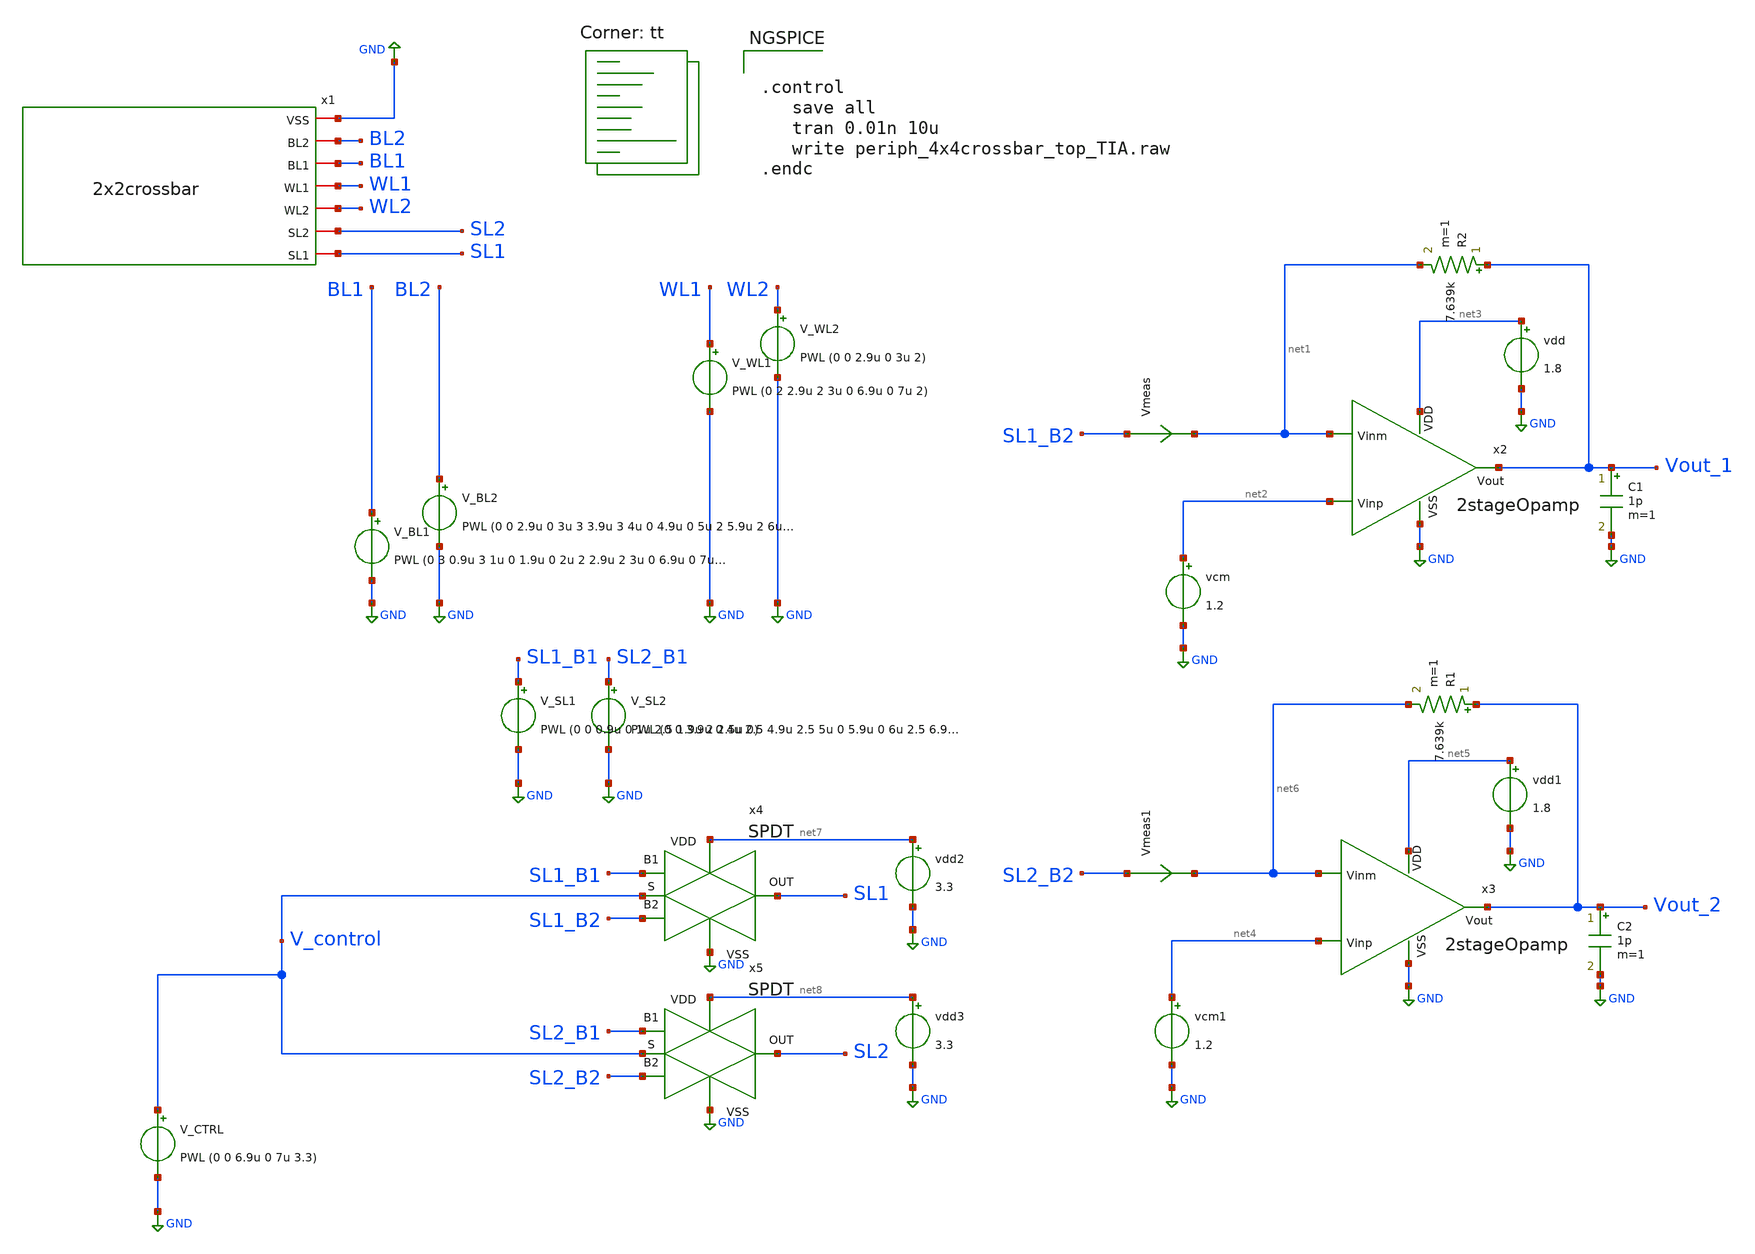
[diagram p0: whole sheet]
** sch_path: xschem/test/xschem/periph_4x4crossbar_top_TIA.sch
* StefanSchippers/xschem_sky130/sky130_fd_pr/reram.sym:
* Copyright 2021 Stefan Frederik Schippers
* Licensed under the Apache License, Version 2.0 (the "License");
**.subckt periph_4x4crossbar_top_TIA
V_BL1 BL1 GND PWL (0 3 0.9u 3 1u 0 1.9u 0 2u 2 2.9u 2 3u 0 6.9u 0 7u 0.2)
V_BL2 BL2 GND PWL (0 0 2.9u 0 3u 3 3.9u 3 4u 0 4.9u 0 5u 2 5.9u 2 6u 0 6.9u 0 7u 0.2)
x1 GND BL2 BL1 WL1 WL2 SL2 SL1 2x2crossbar
V_SL1 SL1_B1 GND PWL (0 0 0.9u 0 1u 2.5 1.9u 2 2.5u 0)
V_SL2 SL2_B1 GND PWL (0 0 3.9u 0 4u 2.5 4.9u 2.5 5u 0 5.9u 0 6u 2.5 6.9u 2.5 7u 0)
V_WL1 WL1 GND PWL (0 2 2.9u 2 3u 0 6.9u 0 7u 2)
V_WL2 WL2 GND PWL (0 0 2.9u 0 3u 2)
x2 net3 net1 net2 Vout_1 GND 2stageOpamp
vcm net2 GND 1.2
vdd net3 GND 1.8
C1 Vout_1 GND 1p m=1
R2 Vout_1 net1 7.639k m=1
x3 net5 net6 net4 Vout_2 GND 2stageOpamp
vcm1 net4 GND 1.2
vdd1 net5 GND 1.8
C2 Vout_2 GND 1p m=1
R1 Vout_2 net6 7.639k m=1
x4 net7 GND SL1_B2 V_control SL1_B1 SL1 SPDT
x5 net8 GND SL2_B2 V_control SL2_B1 SL2 SPDT
V_CTRL V_control GND PWL (0 0 6.9u 0 7u 3.3)
vdd2 net7 GND 3.3
vdd3 net8 GND 3.3
Vmeas SL1_B2 net1 0
.save i(vmeas)
Vmeas1 SL2_B2 net6 0
.save i(vmeas1)
**** begin user architecture code
.lib $::SKYWATER_MODELS/sky130.lib.spice tt


.control
   save all
   tran 0.01n 10u
   write periph_4x4crossbar_top_TIA.raw
.endc


**** end user architecture code
**.ends

* expanding   symbol:  2x2crossbar.sym # of pins=7
** sym_path: 2x2crossbar.sym
** sch_path: 2x2crossbar.sch
.subckt 2x2crossbar VSS BL2 BL1 WL1 WL2 SL2 SL1
*.iopin BL2
*.iopin BL1
*.iopin WL1
*.iopin WL2
*.iopin SL1
*.iopin SL2
*.iopin VSS
x1 BL1 WL1 SL1 VSS 1T1R
x2 BL2 WL1 SL2 VSS 1T1R
x3 BL1 WL2 SL1 VSS 1T1R
x4 BL2 WL2 SL2 VSS 1T1R
.ends


* expanding   symbol:  amplifiers/dec24/2stageOpamp.sym # of pins=5
** sym_path: amplifiers/dec24/2stageOpamp.sym
** sch_path: amplifiers/dec24/2stageOpamp.sch
.subckt 2stageOpamp VDD Vinm Vinp Vout VSS
*.ipin Vinm
*.ipin Vinp
*.opin Vout
*.ipin VSS
*.ipin VDD
XM8 Vout net1 VSS VSS sky130_fd_pr__nfet_01v8 L=1 W=6 nf=1 ad='int((nf+1)/2) * W/nf * 0.29' as='int((nf+2)/2) * W/nf * 0.29'
+ pd='2*int((nf+1)/2) * (W/nf + 0.29)' ps='2*int((nf+2)/2) * (W/nf + 0.29)' nrd='0.29 / W' nrs='0.29 / W'
+ sa=0 sb=0 sd=0 mult=8 m=8
XM2 Vout Vb1 VDD VDD sky130_fd_pr__pfet_01v8_lvt L=1 W=9 nf=1 ad='int((nf+1)/2) * W/nf * 0.29' as='int((nf+2)/2) * W/nf * 0.29'
+ pd='2*int((nf+1)/2) * (W/nf + 0.29)' ps='2*int((nf+2)/2) * (W/nf + 0.29)' nrd='0.29 / W' nrs='0.29 / W'
+ sa=0 sb=0 sd=0 mult=3 m=3
XM5 net5 Vb3 net6 VSS sky130_fd_pr__nfet_01v8 L=1 W=4 nf=1 ad='int((nf+1)/2) * W/nf * 0.29' as='int((nf+2)/2) * W/nf * 0.29'
+ pd='2*int((nf+1)/2) * (W/nf + 0.29)' ps='2*int((nf+2)/2) * (W/nf + 0.29)' nrd='0.29 / W' nrs='0.29 / W'
+ sa=0 sb=0 sd=0 mult=3 m=3
XM17 net1 Vb3 net7 VSS sky130_fd_pr__nfet_01v8 L=1 W=4 nf=1 ad='int((nf+1)/2) * W/nf * 0.29' as='int((nf+2)/2) * W/nf * 0.29'
+ pd='2*int((nf+1)/2) * (W/nf + 0.29)' ps='2*int((nf+2)/2) * (W/nf + 0.29)' nrd='0.29 / W' nrs='0.29 / W'
+ sa=0 sb=0 sd=0 mult=3 m=3
XM3 net6 net5 VSS VSS sky130_fd_pr__nfet_01v8 L=1 W=8 nf=1 ad='int((nf+1)/2) * W/nf * 0.29' as='int((nf+2)/2) * W/nf * 0.29'
+ pd='2*int((nf+1)/2) * (W/nf + 0.29)' ps='2*int((nf+2)/2) * (W/nf + 0.29)' nrd='0.29 / W' nrs='0.29 / W'
+ sa=0 sb=0 sd=0 mult=1 m=1
XM19 net7 net5 VSS VSS sky130_fd_pr__nfet_01v8 L=1 W=8 nf=1 ad='int((nf+1)/2) * W/nf * 0.29' as='int((nf+2)/2) * W/nf * 0.29'
+ pd='2*int((nf+1)/2) * (W/nf + 0.29)' ps='2*int((nf+2)/2) * (W/nf + 0.29)' nrd='0.29 / W' nrs='0.29 / W'
+ sa=0 sb=0 sd=0 mult=1 m=1
V1 Vb1 GND 1.1
V2 Vb2 GND 0.7
V3 Vb3 GND 0.9
XM11 net8 Vb1 VDD VDD sky130_fd_pr__pfet_01v8_lvt L=1 W=9 nf=1 ad='int((nf+1)/2) * W/nf * 0.29' as='int((nf+2)/2) * W/nf * 0.29'
+ pd='2*int((nf+1)/2) * (W/nf + 0.29)' ps='2*int((nf+2)/2) * (W/nf + 0.29)' nrd='0.29 / W' nrs='0.29 / W'
+ sa=0 sb=0 sd=0 mult=2 m=2
XM1 net6 Vinm net8 VDD sky130_fd_pr__pfet_01v8_lvt L=1 W=8 nf=1 ad='int((nf+1)/2) * W/nf * 0.29' as='int((nf+2)/2) * W/nf * 0.29'
+ pd='2*int((nf+1)/2) * (W/nf + 0.29)' ps='2*int((nf+2)/2) * (W/nf + 0.29)' nrd='0.29 / W' nrs='0.29 / W'
+ sa=0 sb=0 sd=0 mult=3 m=3
XM15 net7 Vinp net8 VDD sky130_fd_pr__pfet_01v8_lvt L=1 W=8 nf=1 ad='int((nf+1)/2) * W/nf * 0.29' as='int((nf+2)/2) * W/nf * 0.29'
+ pd='2*int((nf+1)/2) * (W/nf + 0.29)' ps='2*int((nf+2)/2) * (W/nf + 0.29)' nrd='0.29 / W' nrs='0.29 / W'
+ sa=0 sb=0 sd=0 mult=3 m=3
XM7 net3 Vb1 VDD VDD sky130_fd_pr__pfet_01v8_lvt L=1 W=9 nf=1 ad='int((nf+1)/2) * W/nf * 0.29' as='int((nf+2)/2) * W/nf * 0.29'
+ pd='2*int((nf+1)/2) * (W/nf + 0.29)' ps='2*int((nf+2)/2) * (W/nf + 0.29)' nrd='0.29 / W' nrs='0.29 / W'
+ sa=0 sb=0 sd=0 mult=1 m=1
XM21 net4 Vb1 VDD VDD sky130_fd_pr__pfet_01v8_lvt L=1 W=9 nf=1 ad='int((nf+1)/2) * W/nf * 0.29' as='int((nf+2)/2) * W/nf * 0.29'
+ pd='2*int((nf+1)/2) * (W/nf + 0.29)' ps='2*int((nf+2)/2) * (W/nf + 0.29)' nrd='0.29 / W' nrs='0.29 / W'
+ sa=0 sb=0 sd=0 mult=1 m=1
XM9 net5 Vb2 net3 VDD sky130_fd_pr__pfet_01v8_lvt L=1 W=9 nf=1 ad='int((nf+1)/2) * W/nf * 0.29' as='int((nf+2)/2) * W/nf * 0.29'
+ pd='2*int((nf+1)/2) * (W/nf + 0.29)' ps='2*int((nf+2)/2) * (W/nf + 0.29)' nrd='0.29 / W' nrs='0.29 / W'
+ sa=0 sb=0 sd=0 mult=1 m=1
XM23 net1 Vb2 net4 VDD sky130_fd_pr__pfet_01v8_lvt L=1 W=9 nf=1 ad='int((nf+1)/2) * W/nf * 0.29' as='int((nf+2)/2) * W/nf * 0.29'
+ pd='2*int((nf+1)/2) * (W/nf + 0.29)' ps='2*int((nf+2)/2) * (W/nf + 0.29)' nrd='0.29 / W' nrs='0.29 / W'
+ sa=0 sb=0 sd=0 mult=1 m=1
XC4 net2 Vout sky130_fd_pr__cap_mim_m3_2 W=7 L=7 MF=4 m=4
R4 net1 net2 7k m=1
.ends


* expanding   symbol:  SPDT.sym # of pins=6
** sym_path: xschem/test/xschem/SPDT.sym
** sch_path: xschem/test/xschem/SPDT.sch
.subckt SPDT VDD VSS B2 S B1 OUT
*.ipin S
*.ipin VDD
*.ipin VSS
*.iopin OUT
*.iopin B1
*.iopin B2
XM1 OUT net1 B2 VSS sky130_fd_pr__nfet_g5v0d10v5 L=0.5 W=15 nf=1 ad='int((nf+1)/2) * W/nf * 0.29' as='int((nf+2)/2) * W/nf * 0.29'
+ pd='2*int((nf+1)/2) * (W/nf + 0.29)' ps='2*int((nf+2)/2) * (W/nf + 0.29)' nrd='0.29 / W' nrs='0.29 / W'
+ sa=0 sb=0 sd=0 mult=1 m=1
XM2 B2 net2 OUT VDD sky130_fd_pr__pfet_g5v0d10v5 L=0.5 W=15 nf=1 ad='int((nf+1)/2) * W/nf * 0.29' as='int((nf+2)/2) * W/nf * 0.29'
+ pd='2*int((nf+1)/2) * (W/nf + 0.29)' ps='2*int((nf+2)/2) * (W/nf + 0.29)' nrd='0.29 / W' nrs='0.29 / W'
+ sa=0 sb=0 sd=0 mult=1 m=1
XM3 OUT net2 B1 VSS sky130_fd_pr__nfet_g5v0d10v5 L=0.5 W=15 nf=1 ad='int((nf+1)/2) * W/nf * 0.29' as='int((nf+2)/2) * W/nf * 0.29'
+ pd='2*int((nf+1)/2) * (W/nf + 0.29)' ps='2*int((nf+2)/2) * (W/nf + 0.29)' nrd='0.29 / W' nrs='0.29 / W'
+ sa=0 sb=0 sd=0 mult=1 m=1
XM4 B1 net1 OUT VDD sky130_fd_pr__pfet_g5v0d10v5 L=0.5 W=15 nf=1 ad='int((nf+1)/2) * W/nf * 0.29' as='int((nf+2)/2) * W/nf * 0.29'
+ pd='2*int((nf+1)/2) * (W/nf + 0.29)' ps='2*int((nf+2)/2) * (W/nf + 0.29)' nrd='0.29 / W' nrs='0.29 / W'
+ sa=0 sb=0 sd=0 mult=1 m=1
XM5 net2 S VSS VSS sky130_fd_pr__nfet_g5v0d10v5 L=0.5 W=1 nf=1 ad='int((nf+1)/2) * W/nf * 0.29' as='int((nf+2)/2) * W/nf * 0.29'
+ pd='2*int((nf+1)/2) * (W/nf + 0.29)' ps='2*int((nf+2)/2) * (W/nf + 0.29)' nrd='0.29 / W' nrs='0.29 / W'
+ sa=0 sb=0 sd=0 mult=1 m=1
XM6 net2 S VDD VDD sky130_fd_pr__pfet_g5v0d10v5 L=0.5 W=1 nf=1 ad='int((nf+1)/2) * W/nf * 0.29' as='int((nf+2)/2) * W/nf * 0.29'
+ pd='2*int((nf+1)/2) * (W/nf + 0.29)' ps='2*int((nf+2)/2) * (W/nf + 0.29)' nrd='0.29 / W' nrs='0.29 / W'
+ sa=0 sb=0 sd=0 mult=1 m=1
XM7 net1 net2 VSS VSS sky130_fd_pr__nfet_g5v0d10v5 L=0.5 W=1 nf=1 ad='int((nf+1)/2) * W/nf * 0.29' as='int((nf+2)/2) * W/nf * 0.29'
+ pd='2*int((nf+1)/2) * (W/nf + 0.29)' ps='2*int((nf+2)/2) * (W/nf + 0.29)' nrd='0.29 / W' nrs='0.29 / W'
+ sa=0 sb=0 sd=0 mult=1 m=1
XM8 net1 net2 VDD VDD sky130_fd_pr__pfet_g5v0d10v5 L=0.5 W=1 nf=1 ad='int((nf+1)/2) * W/nf * 0.29' as='int((nf+2)/2) * W/nf * 0.29'
+ pd='2*int((nf+1)/2) * (W/nf + 0.29)' ps='2*int((nf+2)/2) * (W/nf + 0.29)' nrd='0.29 / W' nrs='0.29 / W'
+ sa=0 sb=0 sd=0 mult=1 m=1
.ends


* expanding   symbol:  1T1R.sym # of pins=4
** sym_path: xschem/test/xschem/1T1R.sym
** sch_path: xschem/test/xschem/1T1R.sch
.subckt 1T1R BL WL SL VSS
*.iopin SL
*.iopin WL
*.iopin BL
*.iopin VSS
XR1 BL net1 sky130_fd_pr_reram__reram_cell Tfilament_0=3.8e-9
XM1 net1 WL SL VSS sky130_fd_pr__nfet_g5v0d10v5 L=0.5 W=7 nf=1 ad='int((nf+1)/2) * W/nf * 0.29' as='int((nf+2)/2) * W/nf * 0.29'
+ pd='2*int((nf+1)/2) * (W/nf + 0.29)' ps='2*int((nf+2)/2) * (W/nf + 0.29)' nrd='0.29 / W' nrs='0.29 / W'
+ sa=0 sb=0 sd=0 mult=1 m=1
.ends

.GLOBAL GND
**** begin user architecture code

.subckt sky130_fd_pr_reram__reram_cell TE BE Tfilament_0=3.3e-9 area_ox=0.1024e-12
N1 TE BE nFilament sky130_fd_pr_reram__reram_model
.ic v(nFilament)={Tfilament_0*1.0e9}
.ends sky130_fd_pr_reram__reram_cell

.model sky130_fd_pr_reram__reram_model sky130_fd_pr_reram__reram_module  area_ox = 0.1024e-12  Tox =
+ 5.0  Tfilament_max = 4.9  Tfilament_min = 3.3  Eact_generation = 1.501  Eact_recombination  = 1.500
+  I_k1  = 6.140e-5  Tfilament_ref = 4.7249  V_ref = 0.430  velocity_k1 = 150  gamma_k0  = 16.5  gamma_k1
+  = -1.25  Temperature_0 = 300  C_thermal = 3.1825e-16  tau_thermal = 0.23e-9  t_step  = 1.0e-9
+  smoothing = 1e-7  Kclip = 200

.control
pre_osdi $SKYWATER_MODELS/sky130_fd_pr_reram__reram_module.osdi
.endc

**** end user architecture code
.end
